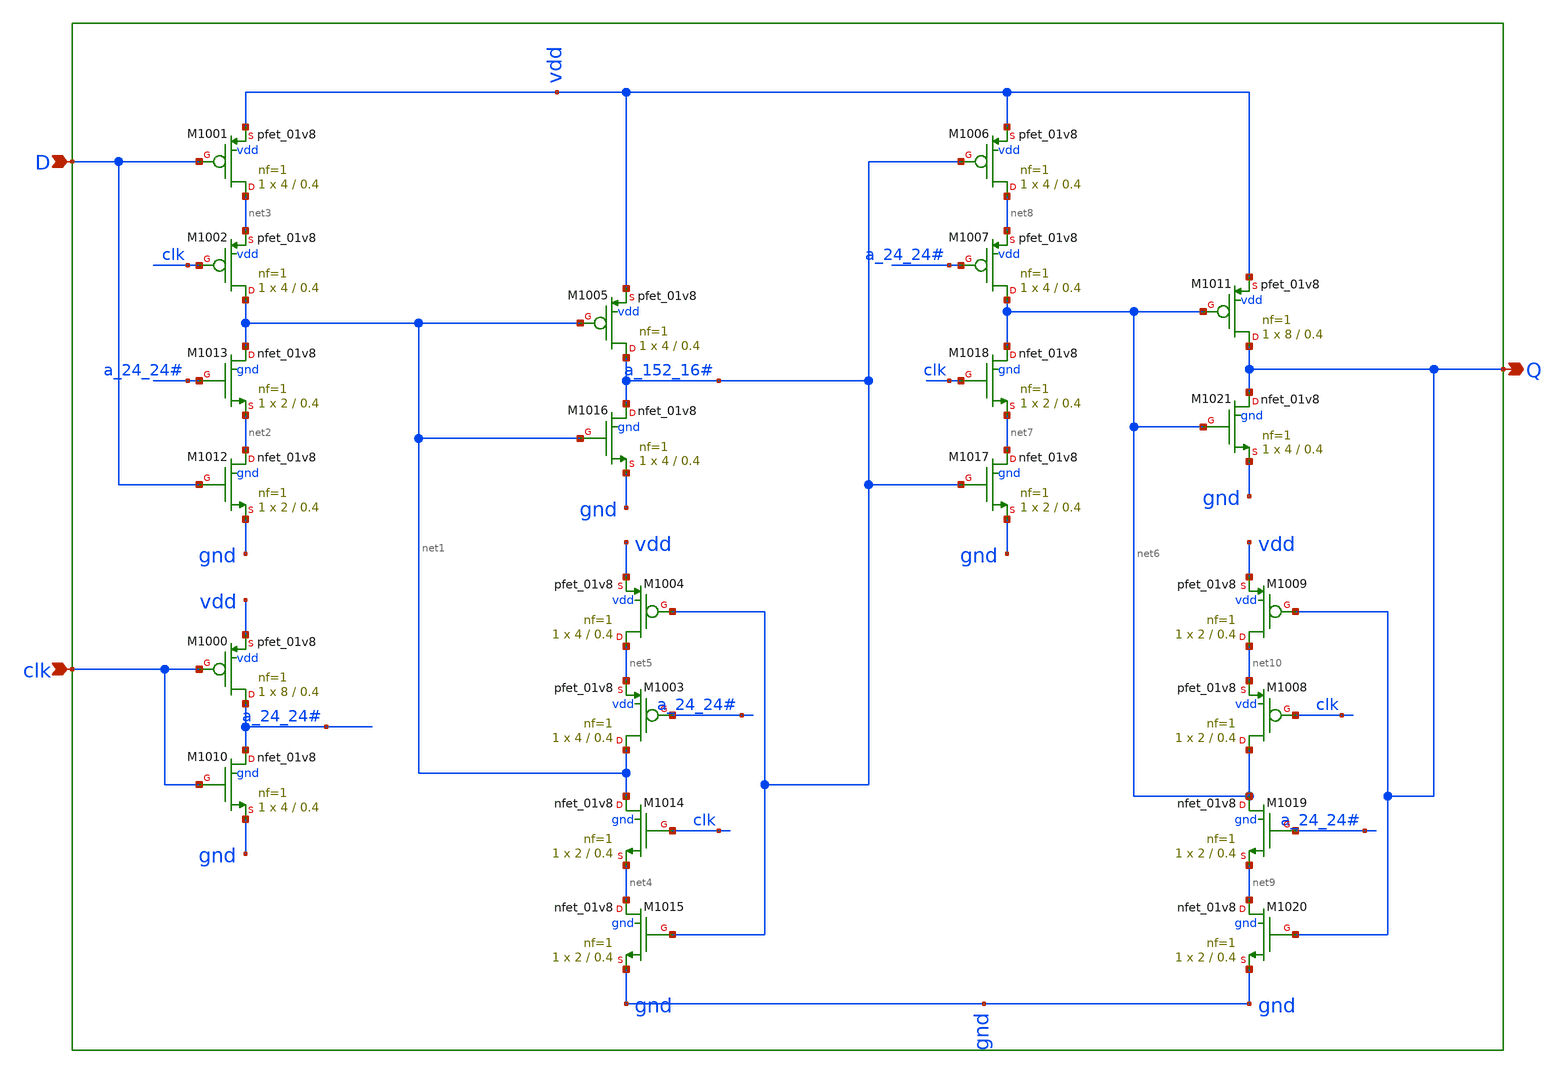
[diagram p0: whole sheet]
** sch_path: sram_2_64_scn4m/dff.sch
**.subckt dff D clk Q
*.ipin D
*.ipin clk
*.opin Q
XM1002 net1 clk net3 vdd sky130_fd_pr__pfet_01v8 L=0.4 W=4 nf=1 ad='int((nf+1)/2) * W/nf * 0.29' as='int((nf+2)/2) * W/nf * 0.29'
+ pd='2*int((nf+1)/2) * (W/nf + 0.29)' ps='2*int((nf+2)/2) * (W/nf + 0.29)' nrd='0.29 / W' nrs='0.29 / W'
+ sa=0 sb=0 sd=0 mult=1 m=1
XM1001 net3 D vdd vdd sky130_fd_pr__pfet_01v8 L=0.4 W=4 nf=1 ad='int((nf+1)/2) * W/nf * 0.29' as='int((nf+2)/2) * W/nf * 0.29'
+ pd='2*int((nf+1)/2) * (W/nf + 0.29)' ps='2*int((nf+2)/2) * (W/nf + 0.29)' nrd='0.29 / W' nrs='0.29 / W'
+ sa=0 sb=0 sd=0 mult=1 m=1
XM1000 a_24_24# clk vdd vdd sky130_fd_pr__pfet_01v8 L=0.4 W=8 nf=1 ad='int((nf+1)/2) * W/nf * 0.29' as='int((nf+2)/2) * W/nf * 0.29'
+ pd='2*int((nf+1)/2) * (W/nf + 0.29)' ps='2*int((nf+2)/2) * (W/nf + 0.29)' nrd='0.29 / W' nrs='0.29 / W'
+ sa=0 sb=0 sd=0 mult=1 m=1
XM1005 a_152_16# net1 vdd vdd sky130_fd_pr__pfet_01v8 L=0.4 W=4 nf=1 ad='int((nf+1)/2) * W/nf * 0.29'
+ as='int((nf+2)/2) * W/nf * 0.29' pd='2*int((nf+1)/2) * (W/nf + 0.29)' ps='2*int((nf+2)/2) * (W/nf + 0.29)'
+ nrd='0.29 / W' nrs='0.29 / W' sa=0 sb=0 sd=0 mult=1 m=1
XM1003 net1 a_24_24# net5 vdd sky130_fd_pr__pfet_01v8 L=0.4 W=4 nf=1 ad='int((nf+1)/2) * W/nf * 0.29'
+ as='int((nf+2)/2) * W/nf * 0.29' pd='2*int((nf+1)/2) * (W/nf + 0.29)' ps='2*int((nf+2)/2) * (W/nf + 0.29)'
+ nrd='0.29 / W' nrs='0.29 / W' sa=0 sb=0 sd=0 mult=1 m=1
XM1004 net5 a_152_16# vdd vdd sky130_fd_pr__pfet_01v8 L=0.4 W=4 nf=1 ad='int((nf+1)/2) * W/nf * 0.29'
+ as='int((nf+2)/2) * W/nf * 0.29' pd='2*int((nf+1)/2) * (W/nf + 0.29)' ps='2*int((nf+2)/2) * (W/nf + 0.29)'
+ nrd='0.29 / W' nrs='0.29 / W' sa=0 sb=0 sd=0 mult=1 m=1
XM1007 net6 a_24_24# net8 vdd sky130_fd_pr__pfet_01v8 L=0.4 W=4 nf=1 ad='int((nf+1)/2) * W/nf * 0.29'
+ as='int((nf+2)/2) * W/nf * 0.29' pd='2*int((nf+1)/2) * (W/nf + 0.29)' ps='2*int((nf+2)/2) * (W/nf + 0.29)'
+ nrd='0.29 / W' nrs='0.29 / W' sa=0 sb=0 sd=0 mult=1 m=1
XM1006 net8 a_152_16# vdd vdd sky130_fd_pr__pfet_01v8 L=0.4 W=4 nf=1 ad='int((nf+1)/2) * W/nf * 0.29'
+ as='int((nf+2)/2) * W/nf * 0.29' pd='2*int((nf+1)/2) * (W/nf + 0.29)' ps='2*int((nf+2)/2) * (W/nf + 0.29)'
+ nrd='0.29 / W' nrs='0.29 / W' sa=0 sb=0 sd=0 mult=1 m=1
XM1011 Q net6 vdd vdd sky130_fd_pr__pfet_01v8 L=0.4 W=8 nf=1 ad='int((nf+1)/2) * W/nf * 0.29' as='int((nf+2)/2) * W/nf * 0.29'
+ pd='2*int((nf+1)/2) * (W/nf + 0.29)' ps='2*int((nf+2)/2) * (W/nf + 0.29)' nrd='0.29 / W' nrs='0.29 / W'
+ sa=0 sb=0 sd=0 mult=1 m=1
XM1008 net6 clk net10 vdd sky130_fd_pr__pfet_01v8 L=0.4 W=2 nf=1 ad='int((nf+1)/2) * W/nf * 0.29' as='int((nf+2)/2) * W/nf * 0.29'
+ pd='2*int((nf+1)/2) * (W/nf + 0.29)' ps='2*int((nf+2)/2) * (W/nf + 0.29)' nrd='0.29 / W' nrs='0.29 / W'
+ sa=0 sb=0 sd=0 mult=1 m=1
XM1009 net10 Q vdd vdd sky130_fd_pr__pfet_01v8 L=0.4 W=2 nf=1 ad='int((nf+1)/2) * W/nf * 0.29' as='int((nf+2)/2) * W/nf * 0.29'
+ pd='2*int((nf+1)/2) * (W/nf + 0.29)' ps='2*int((nf+2)/2) * (W/nf + 0.29)' nrd='0.29 / W' nrs='0.29 / W'
+ sa=0 sb=0 sd=0 mult=1 m=1
XM1013 net1 a_24_24# net2 gnd sky130_fd_pr__nfet_01v8 L=0.4 W=2 nf=1 ad='int((nf+1)/2) * W/nf * 0.29'
+ as='int((nf+2)/2) * W/nf * 0.29' pd='2*int((nf+1)/2) * (W/nf + 0.29)' ps='2*int((nf+2)/2) * (W/nf + 0.29)'
+ nrd='0.29 / W' nrs='0.29 / W' sa=0 sb=0 sd=0 mult=1 m=1
XM1012 net2 D gnd gnd sky130_fd_pr__nfet_01v8 L=0.4 W=2 nf=1 ad='int((nf+1)/2) * W/nf * 0.29' as='int((nf+2)/2) * W/nf * 0.29'
+ pd='2*int((nf+1)/2) * (W/nf + 0.29)' ps='2*int((nf+2)/2) * (W/nf + 0.29)' nrd='0.29 / W' nrs='0.29 / W'
+ sa=0 sb=0 sd=0 mult=1 m=1
XM1010 a_24_24# clk gnd gnd sky130_fd_pr__nfet_01v8 L=0.4 W=4 nf=1 ad='int((nf+1)/2) * W/nf * 0.29' as='int((nf+2)/2) * W/nf * 0.29'
+ pd='2*int((nf+1)/2) * (W/nf + 0.29)' ps='2*int((nf+2)/2) * (W/nf + 0.29)' nrd='0.29 / W' nrs='0.29 / W'
+ sa=0 sb=0 sd=0 mult=1 m=1
XM1016 a_152_16# net1 gnd gnd sky130_fd_pr__nfet_01v8 L=0.4 W=4 nf=1 ad='int((nf+1)/2) * W/nf * 0.29'
+ as='int((nf+2)/2) * W/nf * 0.29' pd='2*int((nf+1)/2) * (W/nf + 0.29)' ps='2*int((nf+2)/2) * (W/nf + 0.29)'
+ nrd='0.29 / W' nrs='0.29 / W' sa=0 sb=0 sd=0 mult=1 m=1
XM1014 net1 clk net4 gnd sky130_fd_pr__nfet_01v8 L=0.4 W=2 nf=1 ad='int((nf+1)/2) * W/nf * 0.29' as='int((nf+2)/2) * W/nf * 0.29'
+ pd='2*int((nf+1)/2) * (W/nf + 0.29)' ps='2*int((nf+2)/2) * (W/nf + 0.29)' nrd='0.29 / W' nrs='0.29 / W'
+ sa=0 sb=0 sd=0 mult=1 m=1
XM1015 net4 a_152_16# gnd gnd sky130_fd_pr__nfet_01v8 L=0.4 W=2 nf=1 ad='int((nf+1)/2) * W/nf * 0.29'
+ as='int((nf+2)/2) * W/nf * 0.29' pd='2*int((nf+1)/2) * (W/nf + 0.29)' ps='2*int((nf+2)/2) * (W/nf + 0.29)'
+ nrd='0.29 / W' nrs='0.29 / W' sa=0 sb=0 sd=0 mult=1 m=1
XM1020 net9 Q gnd gnd sky130_fd_pr__nfet_01v8 L=0.4 W=2 nf=1 ad='int((nf+1)/2) * W/nf * 0.29' as='int((nf+2)/2) * W/nf * 0.29'
+ pd='2*int((nf+1)/2) * (W/nf + 0.29)' ps='2*int((nf+2)/2) * (W/nf + 0.29)' nrd='0.29 / W' nrs='0.29 / W'
+ sa=0 sb=0 sd=0 mult=1 m=1
XM1019 net6 a_24_24# net9 gnd sky130_fd_pr__nfet_01v8 L=0.4 W=2 nf=1 ad='int((nf+1)/2) * W/nf * 0.29'
+ as='int((nf+2)/2) * W/nf * 0.29' pd='2*int((nf+1)/2) * (W/nf + 0.29)' ps='2*int((nf+2)/2) * (W/nf + 0.29)'
+ nrd='0.29 / W' nrs='0.29 / W' sa=0 sb=0 sd=0 mult=1 m=1
XM1021 Q net6 gnd gnd sky130_fd_pr__nfet_01v8 L=0.4 W=4 nf=1 ad='int((nf+1)/2) * W/nf * 0.29' as='int((nf+2)/2) * W/nf * 0.29'
+ pd='2*int((nf+1)/2) * (W/nf + 0.29)' ps='2*int((nf+2)/2) * (W/nf + 0.29)' nrd='0.29 / W' nrs='0.29 / W'
+ sa=0 sb=0 sd=0 mult=1 m=1
XM1018 net6 clk net7 gnd sky130_fd_pr__nfet_01v8 L=0.4 W=2 nf=1 ad='int((nf+1)/2) * W/nf * 0.29' as='int((nf+2)/2) * W/nf * 0.29'
+ pd='2*int((nf+1)/2) * (W/nf + 0.29)' ps='2*int((nf+2)/2) * (W/nf + 0.29)' nrd='0.29 / W' nrs='0.29 / W'
+ sa=0 sb=0 sd=0 mult=1 m=1
XM1017 net7 a_152_16# gnd gnd sky130_fd_pr__nfet_01v8 L=0.4 W=2 nf=1 ad='int((nf+1)/2) * W/nf * 0.29'
+ as='int((nf+2)/2) * W/nf * 0.29' pd='2*int((nf+1)/2) * (W/nf + 0.29)' ps='2*int((nf+2)/2) * (W/nf + 0.29)'
+ nrd='0.29 / W' nrs='0.29 / W' sa=0 sb=0 sd=0 mult=1 m=1
**.ends
.end
